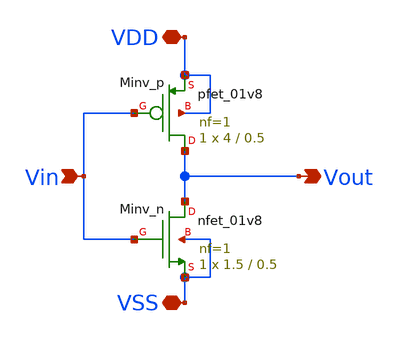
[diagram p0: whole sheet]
** sch_path: xschem/ip_block/logic_gate/inv.sch
**.subckt inv Vin Vout VDD VSS
*.ipin Vin
*.opin Vout
*.iopin VDD
*.iopin VSS
XMinv_n Vout Vin VSS VSS sky130_fd_pr__nfet_01v8 L=0.5 W=1.5 nf=1 ad='int((nf+1)/2) * W/nf * 0.29' as='int((nf+2)/2) * W/nf * 0.29'
+ pd='2*int((nf+1)/2) * (W/nf + 0.29)' ps='2*int((nf+2)/2) * (W/nf + 0.29)' nrd='0.29 / W' nrs='0.29 / W'
+ sa=0 sb=0 sd=0 mult=1 m=1
XMinv_p Vout Vin VDD VDD sky130_fd_pr__pfet_01v8 L=0.5 W=4 nf=1 ad='int((nf+1)/2) * W/nf * 0.29' as='int((nf+2)/2) * W/nf * 0.29'
+ pd='2*int((nf+1)/2) * (W/nf + 0.29)' ps='2*int((nf+2)/2) * (W/nf + 0.29)' nrd='0.29 / W' nrs='0.29 / W'
+ sa=0 sb=0 sd=0 mult=1 m=1
**.ends
.end
